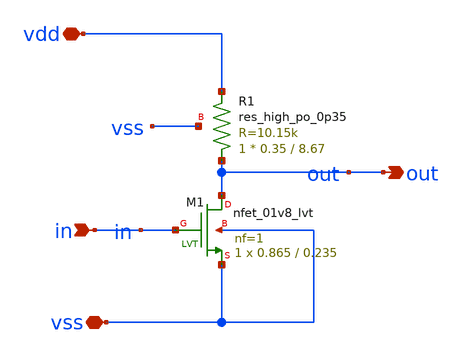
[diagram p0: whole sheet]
** sch_path: ISSCC27/submitted_notebooks/PerfPDN/examples/common_source_amplifier/cs.sch
**.subckt cs vdd vss in out
*.iopin vdd
*.iopin vss
*.ipin in
*.opin out
XR1 out vdd vss sky130_fd_pr__res_high_po_0p35 L=8.67 mult=1 m=1
XM1 out in vss vss sky130_fd_pr__nfet_01v8_lvt L=0.235 W=0.865 nf=1 ad='int(( 1 + 1 ) / 2 ) * 0.865 / 1 * 0.29'
+ as='int(( 1 + 2 ) / 2 ) * 0.865 / 1 * 0.29' pd='2 * int(( 1 + 1 ) / 2 ) * ( 0.865 / 1 + 0.29 )' ps='2 * int(( 1 + 2 ) / 2 ) * ( 0.865 / 1 + 0.29 )'
+ nrd='0.29 / 0.865 ' nrs='0.29 / 0.865 ' sa=0 sb=0 sd=0 mult=1 m=1
**.ends
.end
